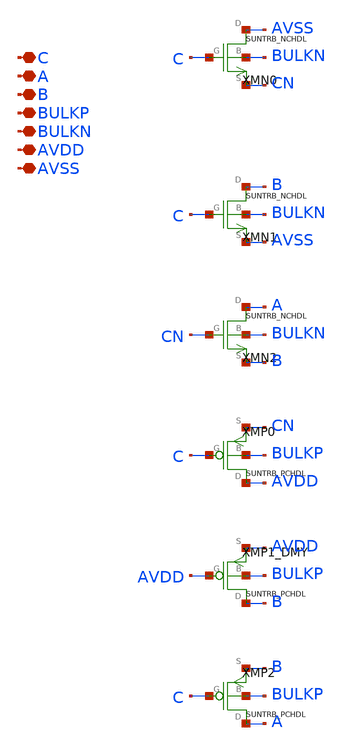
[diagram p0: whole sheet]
** sch_path: ip/sun_trb_sky130nm/design/SUN_TRB_SKY130NM/SUNTRB_TGPD_CV.sch
**.subckt SUNTRB_TGPD_CV C A B BULKP BULKN AVDD AVSS
*.iopin C
*.iopin A
*.iopin B
*.iopin BULKP
*.iopin BULKN
*.iopin AVDD
*.iopin AVSS
XMN0 AVSS C CN BULKN SUNTRB_NCHDL xoffset=0 yoffset=0 angle=0
XMN1 B C AVSS BULKN SUNTRB_NCHDL xoffset=0 yoffset=0 angle=0
XMN2 A CN B BULKN SUNTRB_NCHDL xoffset=0 yoffset=0 angle=0
XMP0 AVDD C CN BULKP SUNTRB_PCHDL xoffset=0 yoffset=0 angle=0
XMP1_DMY B AVDD AVDD BULKP SUNTRB_PCHDL xoffset=0 yoffset=0 angle=0
XMP2 A C B BULKP SUNTRB_PCHDL xoffset=0 yoffset=0 angle=0
**.ends
.end
